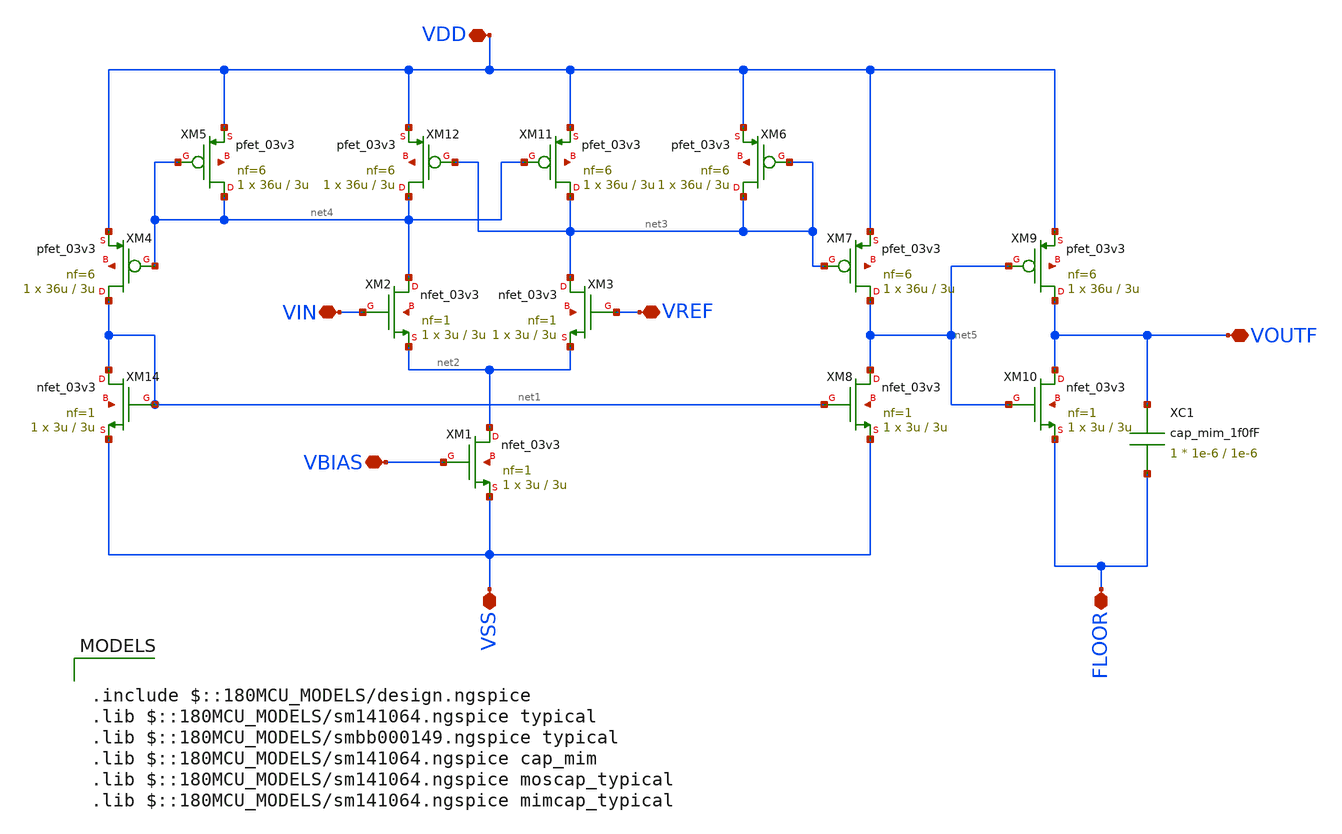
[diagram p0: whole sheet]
** sch_path: src/schematics/comparator/comparator.sch
**.subckt comparator VDD VSS FLOOR VBIAS VIN VREF VOUTF
*.iopin VDD
*.iopin VSS
*.iopin FLOOR
*.iopin VBIAS
*.iopin VIN
*.iopin VREF
*.iopin VOUTF
XM14 net1 net1 VSS net6 nfet_03v3 L=3u W=3u nf=1 ad='int((nf+1)/2) * W/nf * 0.18u' as='int((nf+2)/2) * W/nf * 0.18u'
+ pd='2*int((nf+1)/2) * (W/nf + 0.18u)' ps='2*int((nf+2)/2) * (W/nf + 0.18u)' nrd='0.18u / W' nrs='0.18u / W'
+ sa=0 sb=0 sd=0 m=1
XM1 net2 VBIAS VSS net7 nfet_03v3 L=3u W=3u nf=1 ad='int((nf+1)/2) * W/nf * 0.18u' as='int((nf+2)/2) * W/nf * 0.18u'
+ pd='2*int((nf+1)/2) * (W/nf + 0.18u)' ps='2*int((nf+2)/2) * (W/nf + 0.18u)' nrd='0.18u / W' nrs='0.18u / W'
+ sa=0 sb=0 sd=0 m=1
XM2 net4 VIN net2 net8 nfet_03v3 L=3u W=3u nf=1 ad='int((nf+1)/2) * W/nf * 0.18u' as='int((nf+2)/2) * W/nf * 0.18u'
+ pd='2*int((nf+1)/2) * (W/nf + 0.18u)' ps='2*int((nf+2)/2) * (W/nf + 0.18u)' nrd='0.18u / W' nrs='0.18u / W'
+ sa=0 sb=0 sd=0 m=1
XM3 net3 VREF net2 net9 nfet_03v3 L=3u W=3u nf=1 ad='int((nf+1)/2) * W/nf * 0.18u' as='int((nf+2)/2) * W/nf * 0.18u'
+ pd='2*int((nf+1)/2) * (W/nf + 0.18u)' ps='2*int((nf+2)/2) * (W/nf + 0.18u)' nrd='0.18u / W' nrs='0.18u / W'
+ sa=0 sb=0 sd=0 m=1
XM12 net4 net3 VDD net10 pfet_03v3 L=3u W=36u nf=6 ad='int((nf+1)/2) * W/nf * 0.18u' as='int((nf+2)/2) * W/nf * 0.18u'
+ pd='2*int((nf+1)/2) * (W/nf + 0.18u)' ps='2*int((nf+2)/2) * (W/nf + 0.18u)' nrd='0.18u / W' nrs='0.18u / W'
+ sa=0 sb=0 sd=0 m=1
XM11 net3 net4 VDD net11 pfet_03v3 L=3u W=36u nf=6 ad='int((nf+1)/2) * W/nf * 0.18u' as='int((nf+2)/2) * W/nf * 0.18u'
+ pd='2*int((nf+1)/2) * (W/nf + 0.18u)' ps='2*int((nf+2)/2) * (W/nf + 0.18u)' nrd='0.18u / W' nrs='0.18u / W'
+ sa=0 sb=0 sd=0 m=1
XM4 net1 net4 VDD net12 pfet_03v3 L=3u W=36u nf=6 ad='int((nf+1)/2) * W/nf * 0.18u' as='int((nf+2)/2) * W/nf * 0.18u'
+ pd='2*int((nf+1)/2) * (W/nf + 0.18u)' ps='2*int((nf+2)/2) * (W/nf + 0.18u)' nrd='0.18u / W' nrs='0.18u / W'
+ sa=0 sb=0 sd=0 m=1
XM5 net4 net4 VDD net13 pfet_03v3 L=3u W=36u nf=6 ad='int((nf+1)/2) * W/nf * 0.18u' as='int((nf+2)/2) * W/nf * 0.18u'
+ pd='2*int((nf+1)/2) * (W/nf + 0.18u)' ps='2*int((nf+2)/2) * (W/nf + 0.18u)' nrd='0.18u / W' nrs='0.18u / W'
+ sa=0 sb=0 sd=0 m=1
XM6 net3 net3 VDD net14 pfet_03v3 L=3u W=36u nf=6 ad='int((nf+1)/2) * W/nf * 0.18u' as='int((nf+2)/2) * W/nf * 0.18u'
+ pd='2*int((nf+1)/2) * (W/nf + 0.18u)' ps='2*int((nf+2)/2) * (W/nf + 0.18u)' nrd='0.18u / W' nrs='0.18u / W'
+ sa=0 sb=0 sd=0 m=1
XM7 net5 net3 VDD net15 pfet_03v3 L=3u W=36u nf=6 ad='int((nf+1)/2) * W/nf * 0.18u' as='int((nf+2)/2) * W/nf * 0.18u'
+ pd='2*int((nf+1)/2) * (W/nf + 0.18u)' ps='2*int((nf+2)/2) * (W/nf + 0.18u)' nrd='0.18u / W' nrs='0.18u / W'
+ sa=0 sb=0 sd=0 m=1
XM8 net5 net1 VSS net16 nfet_03v3 L=3u W=3u nf=1 ad='int((nf+1)/2) * W/nf * 0.18u' as='int((nf+2)/2) * W/nf * 0.18u'
+ pd='2*int((nf+1)/2) * (W/nf + 0.18u)' ps='2*int((nf+2)/2) * (W/nf + 0.18u)' nrd='0.18u / W' nrs='0.18u / W'
+ sa=0 sb=0 sd=0 m=1
XM9 VOUTF net5 VDD net17 pfet_03v3 L=3u W=36u nf=6 ad='int((nf+1)/2) * W/nf * 0.18u' as='int((nf+2)/2) * W/nf * 0.18u'
+ pd='2*int((nf+1)/2) * (W/nf + 0.18u)' ps='2*int((nf+2)/2) * (W/nf + 0.18u)' nrd='0.18u / W' nrs='0.18u / W'
+ sa=0 sb=0 sd=0 m=1
XM10 VOUTF net5 FLOOR net18 nfet_03v3 L=3u W=3u nf=1 ad='int((nf+1)/2) * W/nf * 0.18u' as='int((nf+2)/2) * W/nf * 0.18u'
+ pd='2*int((nf+1)/2) * (W/nf + 0.18u)' ps='2*int((nf+2)/2) * (W/nf + 0.18u)' nrd='0.18u / W' nrs='0.18u / W'
+ sa=0 sb=0 sd=0 m=1
XC1 VOUTF FLOOR cap_mim_1f0fF c_width=1e-6 c_length=1e-6 m=1
**** begin user architecture code

.include $::180MCU_MODELS/design.ngspice
.lib $::180MCU_MODELS/sm141064.ngspice typical
.lib $::180MCU_MODELS/smbb000149.ngspice typical
.lib $::180MCU_MODELS/sm141064.ngspice cap_mim
.lib $::180MCU_MODELS/sm141064.ngspice moscap_typical
.lib $::180MCU_MODELS/sm141064.ngspice mimcap_typical

**** end user architecture code
**.ends
.end
